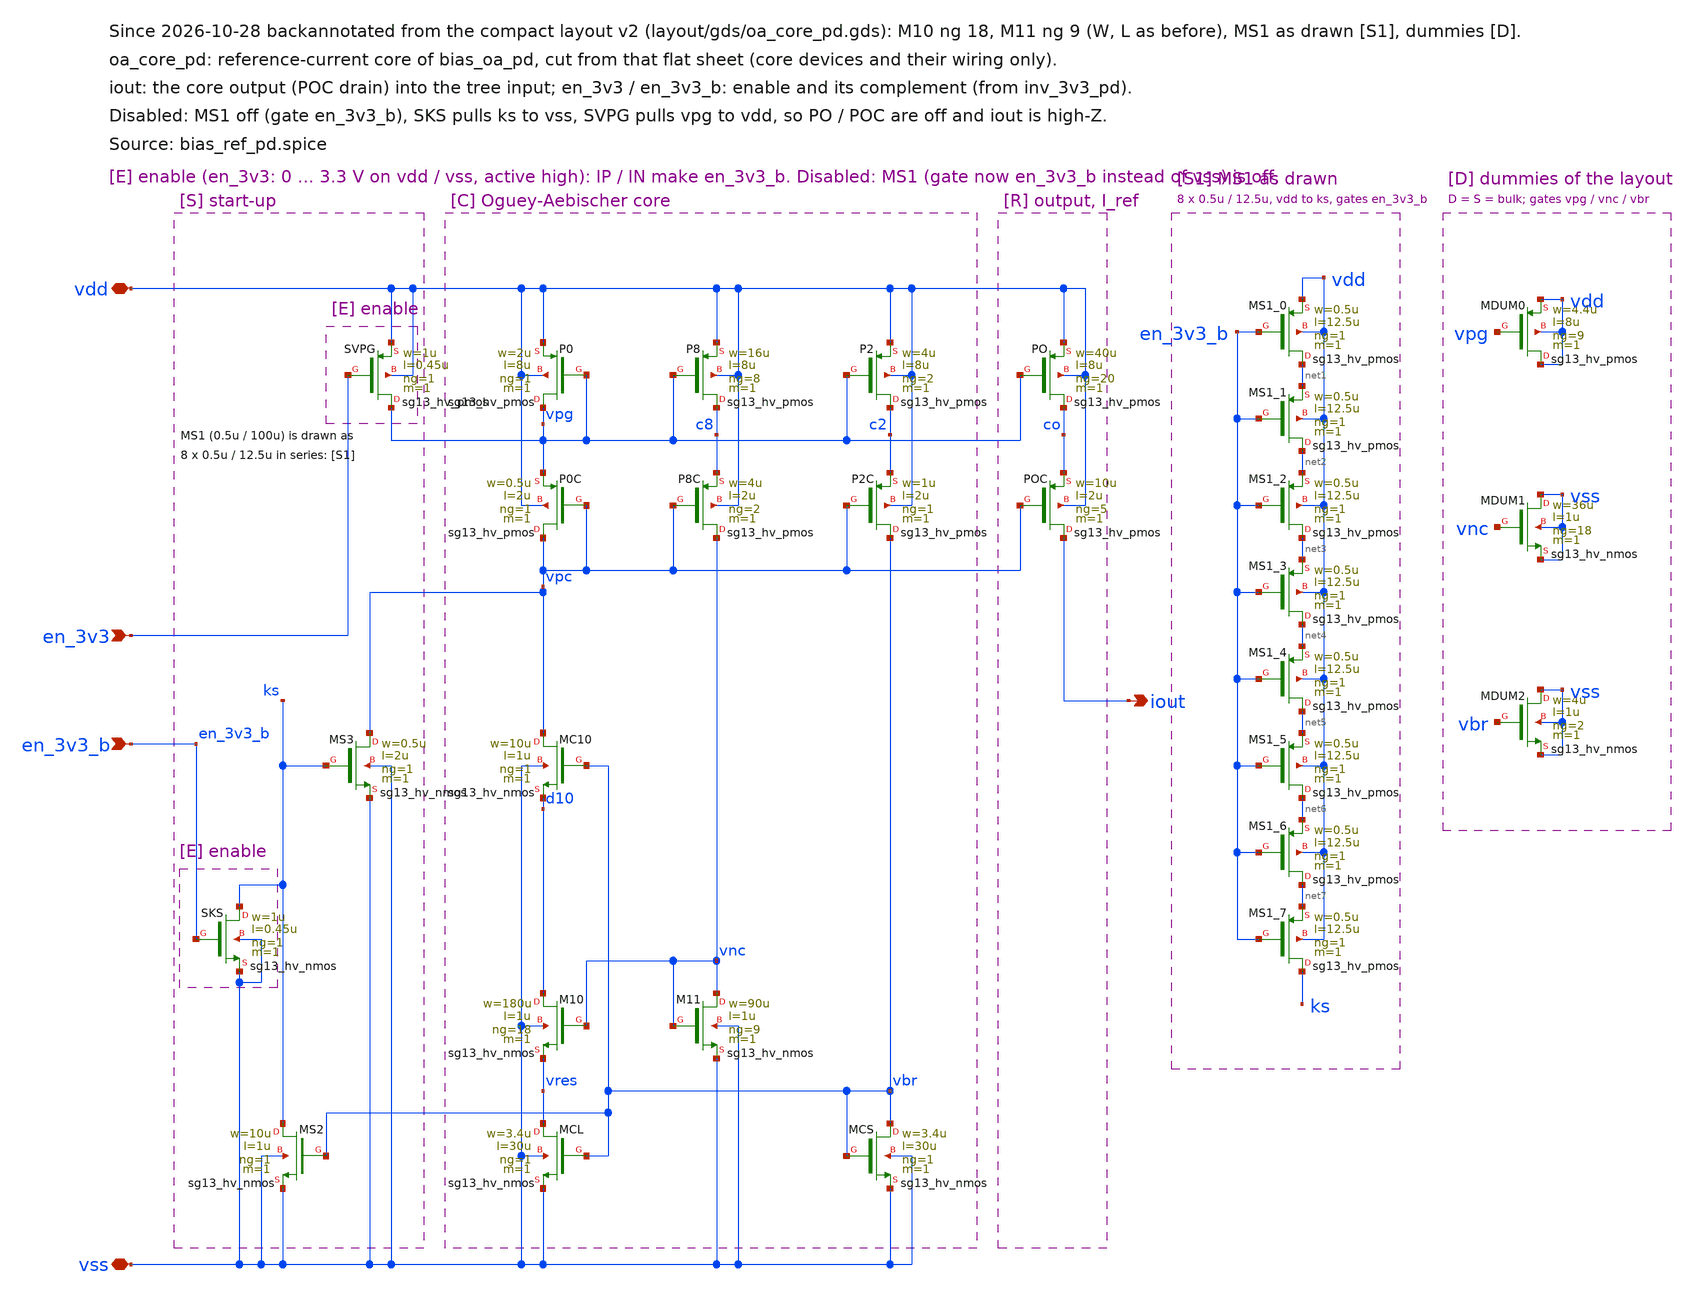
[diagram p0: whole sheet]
** sch_path: macros/oa_core_pd/schematic/xschem/oa_core_pd.sch
**.subckt oa_core_pd vdd vss en_3v3 en_3v3_b iout
*.iopin vdd
*.iopin vss
*.ipin en_3v3
*.ipin en_3v3_b
*.opin iout
XMS2 ks vbr vss vss sg13_hv_nmos w=10u l=1u ng=1 m=1 mm_ok=1
XMS3 vpc ks vss vss sg13_hv_nmos w=0.5u l=2u ng=1 m=1 mm_ok=1
XP0 vpg vpg vdd vdd sg13_hv_pmos w=2u l=8u ng=1 m=1 mm_ok=1
XP0C vpc vpc vpg vdd sg13_hv_pmos w=0.5u l=2u ng=1 m=1 mm_ok=1
XMC10 vpc vbr d10 vss sg13_hv_nmos w=10u l=1u ng=1 m=1 mm_ok=1
XM10 d10 vnc vres vss sg13_hv_nmos w=180u l=1u ng=18 m=1 mm_ok=1
XMCL vres vbr vss vss sg13_hv_nmos w=3.4u l=30u ng=1 m=1 mm_ok=1
XP8 c8 vpg vdd vdd sg13_hv_pmos w=16u l=8u ng=8 m=1 mm_ok=1
XP8C vnc vpc c8 vdd sg13_hv_pmos w=4u l=2u ng=2 m=1 mm_ok=1
XM11 vnc vnc vss vss sg13_hv_nmos w=90u l=1u ng=9 m=1 mm_ok=1
XP2 c2 vpg vdd vdd sg13_hv_pmos w=4u l=8u ng=2 m=1 mm_ok=1
XP2C vbr vpc c2 vdd sg13_hv_pmos w=1u l=2u ng=1 m=1 mm_ok=1
XMCS vbr vbr vss vss sg13_hv_nmos w=3.4u l=30u ng=1 m=1 mm_ok=1
XPO co vpg vdd vdd sg13_hv_pmos w=40u l=8u ng=20 m=1 mm_ok=1
XPOC iout vpc co vdd sg13_hv_pmos w=10u l=2u ng=5 m=1 mm_ok=1
XSKS ks en_3v3_b vss vss sg13_hv_nmos w=1u l=0.45u ng=1 m=1 mm_ok=1
XSVPG vpg en_3v3 vdd vdd sg13_hv_pmos w=1u l=0.45u ng=1 m=1 mm_ok=1
XMS1_0 net1 en_3v3_b vdd vdd sg13_hv_pmos w=0.5u l=12.5u ng=1 m=1 mm_ok=1
XMS1_1 net2 en_3v3_b net1 vdd sg13_hv_pmos w=0.5u l=12.5u ng=1 m=1 mm_ok=1
XMS1_2 net3 en_3v3_b net2 vdd sg13_hv_pmos w=0.5u l=12.5u ng=1 m=1 mm_ok=1
XMS1_3 net4 en_3v3_b net3 vdd sg13_hv_pmos w=0.5u l=12.5u ng=1 m=1 mm_ok=1
XMS1_4 net5 en_3v3_b net4 vdd sg13_hv_pmos w=0.5u l=12.5u ng=1 m=1 mm_ok=1
XMS1_5 net6 en_3v3_b net5 vdd sg13_hv_pmos w=0.5u l=12.5u ng=1 m=1 mm_ok=1
XMS1_6 net7 en_3v3_b net6 vdd sg13_hv_pmos w=0.5u l=12.5u ng=1 m=1 mm_ok=1
XMS1_7 ks en_3v3_b net7 vdd sg13_hv_pmos w=0.5u l=12.5u ng=1 m=1 mm_ok=1
XMDUM0 vdd vpg vdd vdd sg13_hv_pmos w=4.4u l=8u ng=9 m=1 mm_ok=1
XMDUM1 vss vnc vss vss sg13_hv_nmos w=36u l=1u ng=18 m=1 mm_ok=1
XMDUM2 vss vbr vss vss sg13_hv_nmos w=4u l=1u ng=2 m=1 mm_ok=1
**.ends
.end
